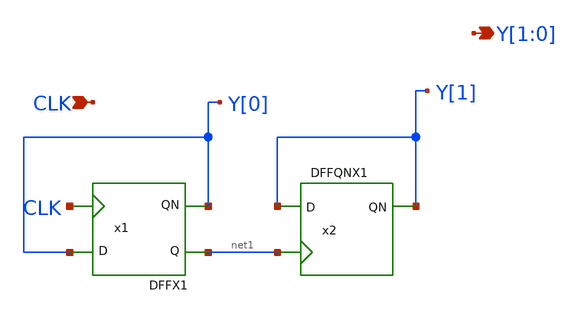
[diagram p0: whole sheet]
** sch_path: current/xschem/Mod4Counter/Mod4Counter.sch
**.subckt Mod4Counter Y[1],Y[0] CLK
*.opin Y[1],Y[0]
*.ipin CLK
x1 net1 Y[0] Y[0] CLK VDD VSS DFFX1
x2 net1 Y[1] Y[1] VDD VSS DFFQNX1
**.ends
.end
